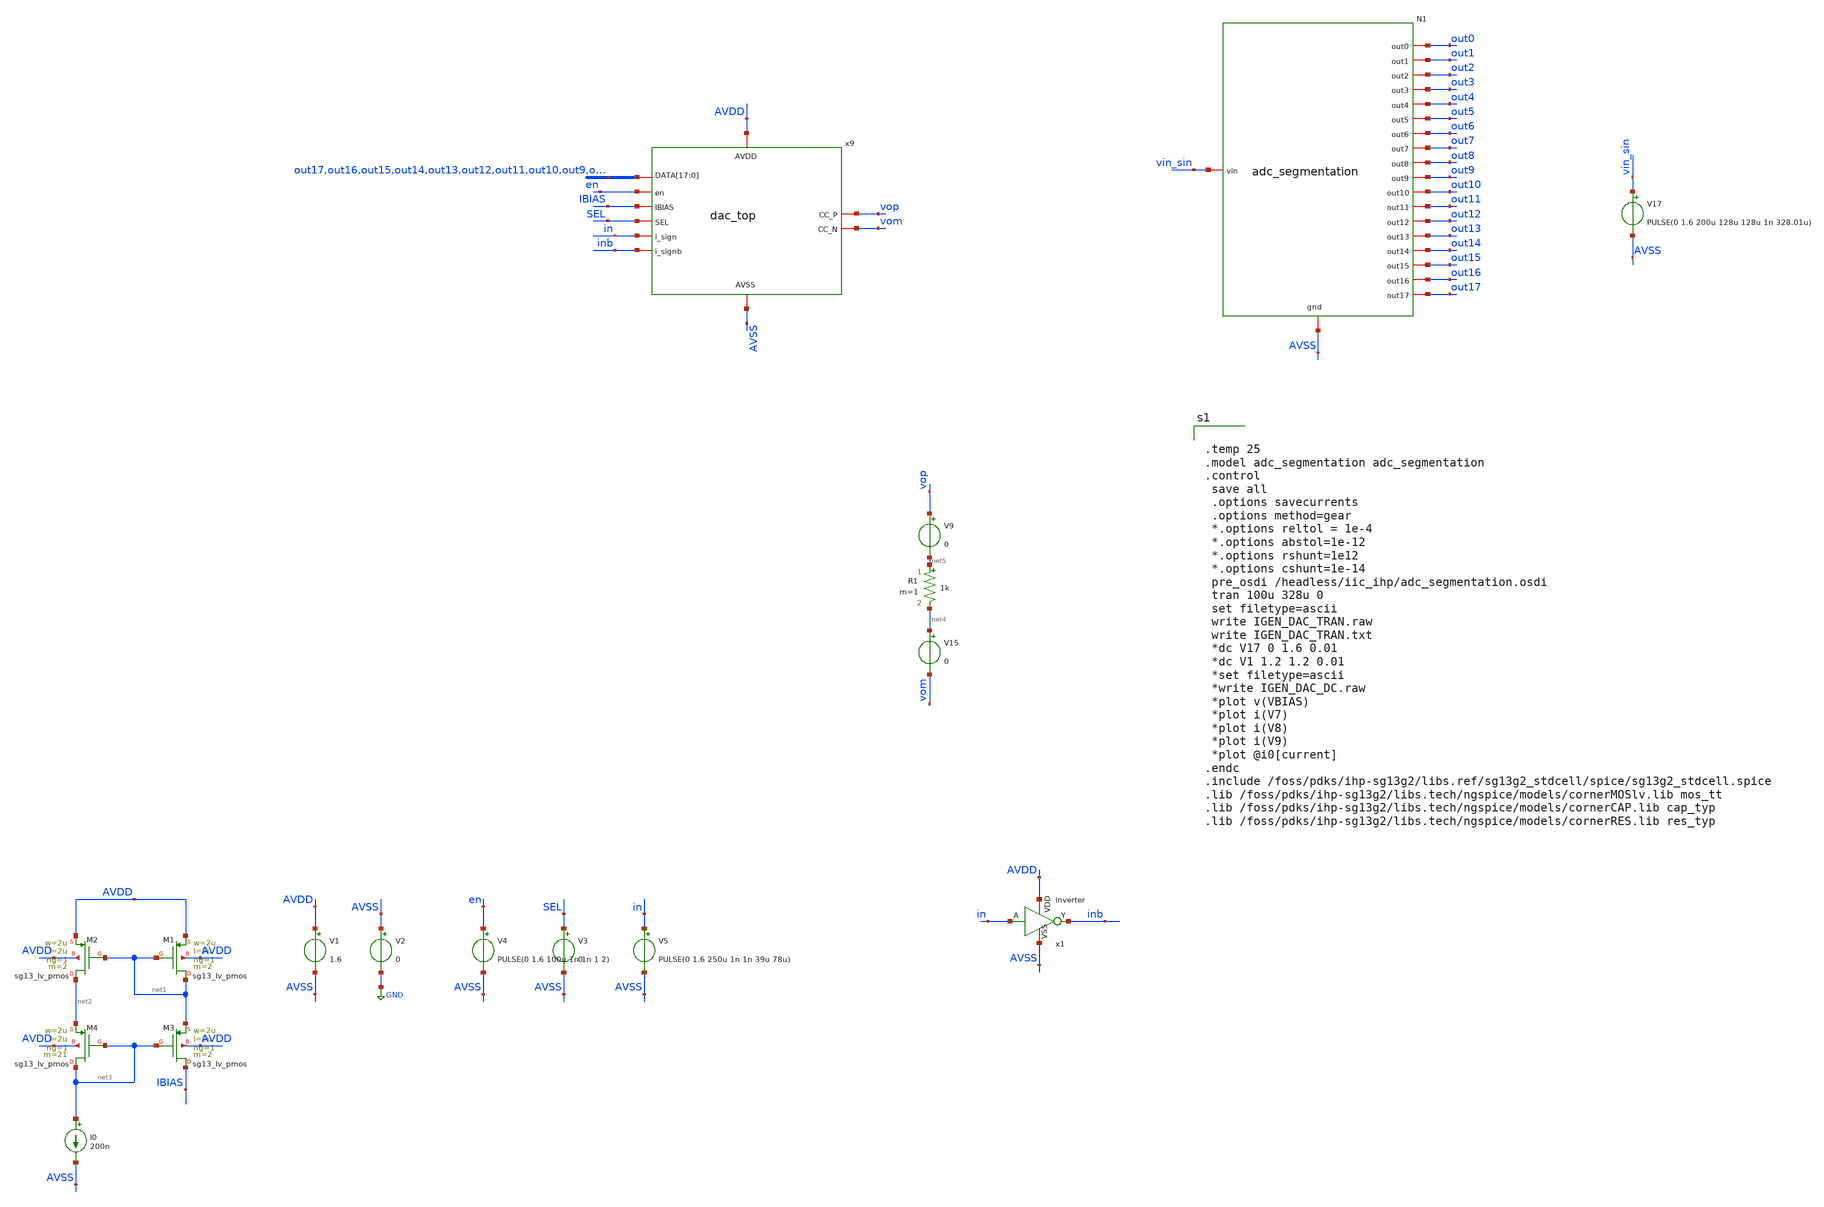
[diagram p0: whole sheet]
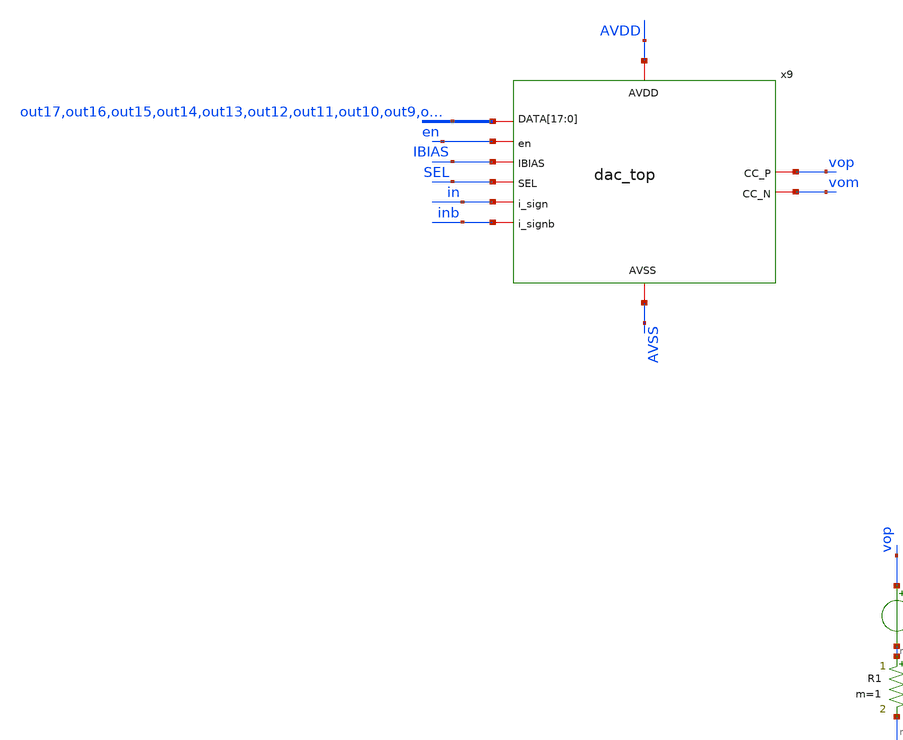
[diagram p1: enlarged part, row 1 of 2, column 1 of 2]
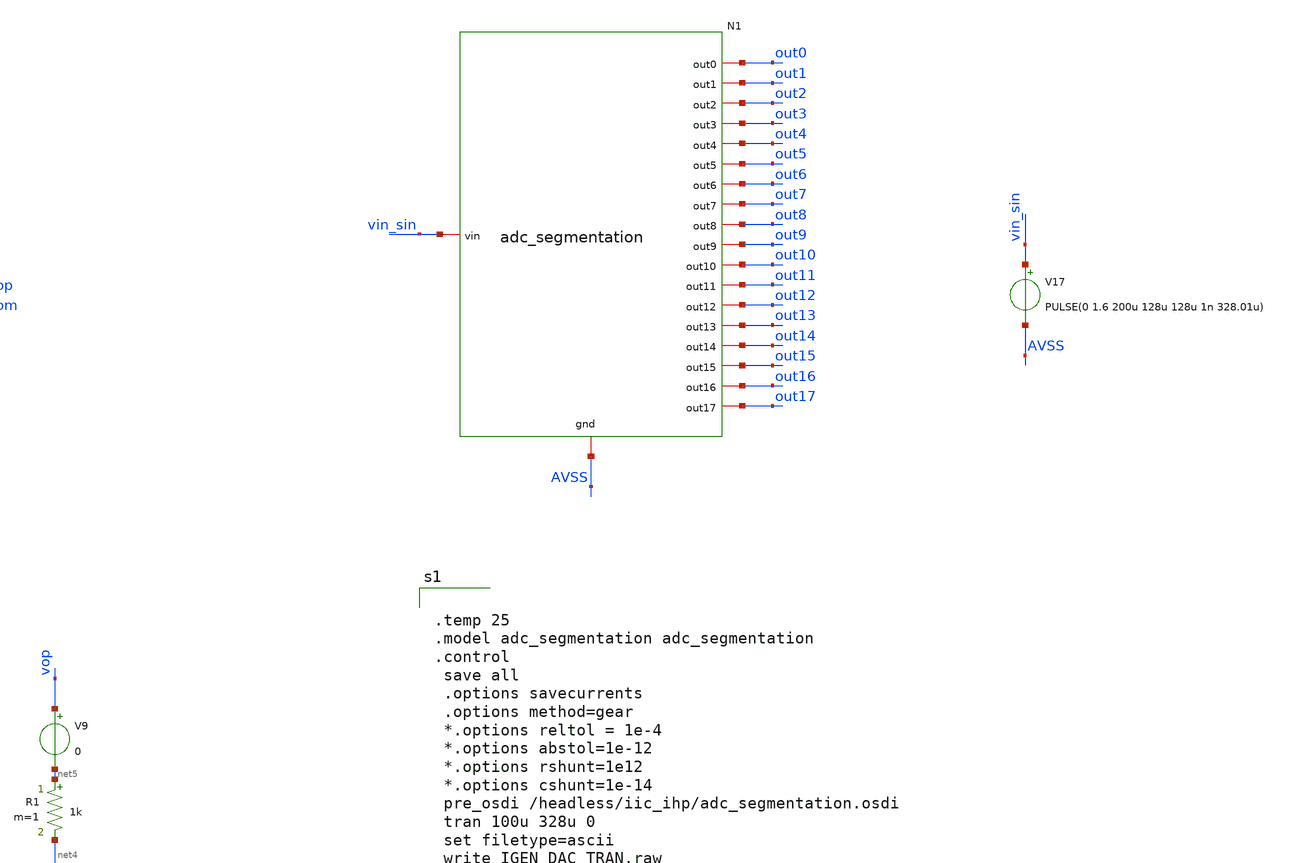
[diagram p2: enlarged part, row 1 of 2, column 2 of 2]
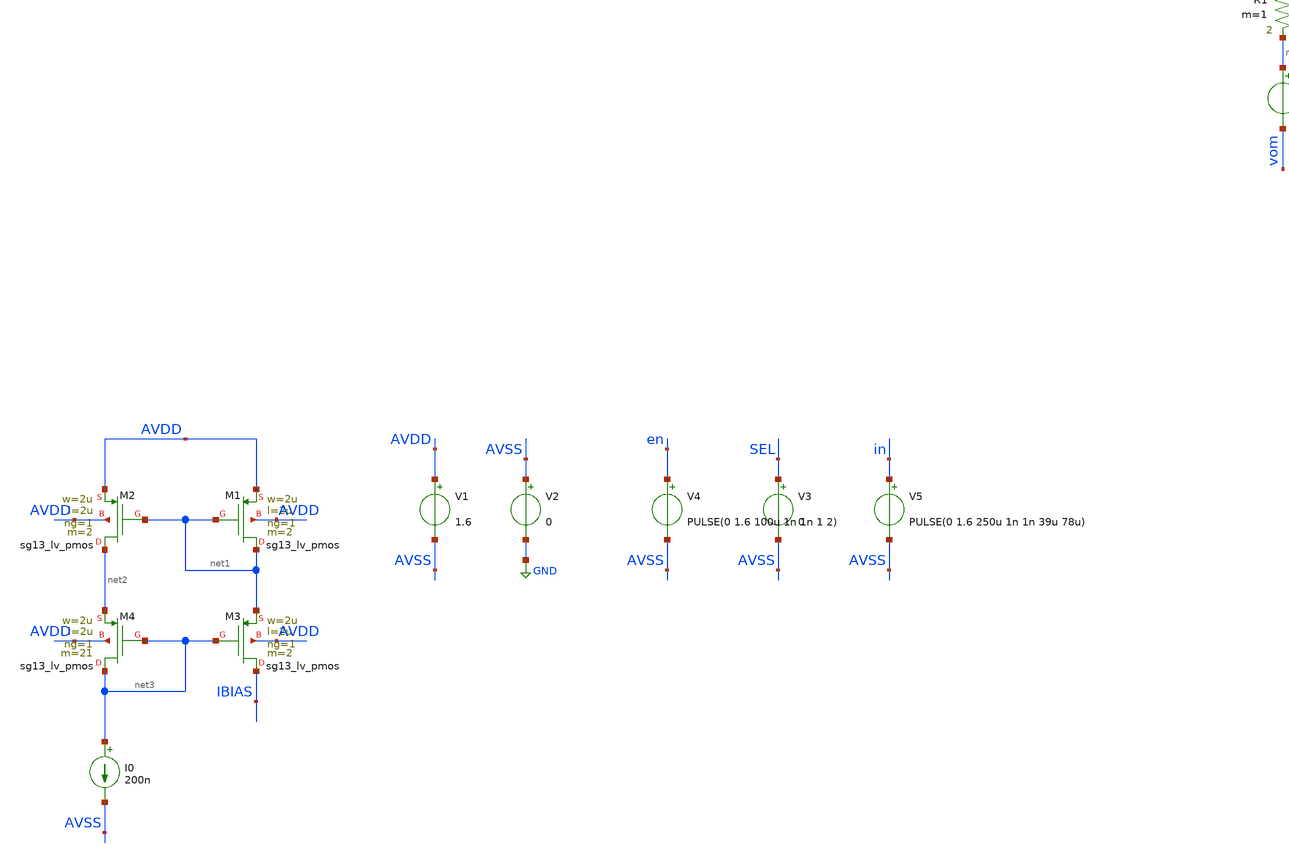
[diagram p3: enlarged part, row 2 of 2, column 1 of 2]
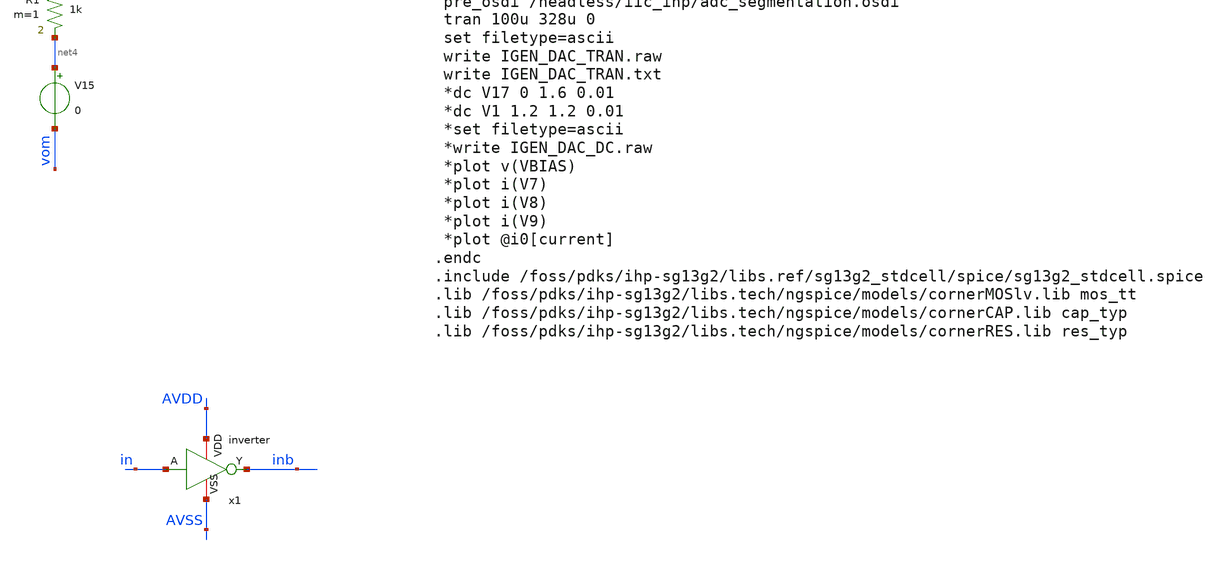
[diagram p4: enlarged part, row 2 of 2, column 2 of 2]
** sch_path: current_generator/analog/DAC/schematics/tb_dac_top.sch
**.subckt tb_dac_top
I0 net3 AVSS 200n
V1 AVDD AVSS 1.6
V2 AVSS GND 0
V3 SEL AVSS 0
XM1 net1 net1 AVDD AVDD sg13_lv_pmos w=2u l=2u ng=1 m=2 mm_ok=1
XM2 net2 net1 AVDD AVDD sg13_lv_pmos w=2u l=2u ng=1 m=2 mm_ok=1
XM3 IBIAS net3 net1 AVDD sg13_lv_pmos w=2u l=2u ng=1 m=2 mm_ok=1
XM4 net3 net3 net2 AVDD sg13_lv_pmos w=2u l=2u ng=1 m=21 mm_ok=1
N1 vin_sin AVSS out0 out10 out11 out1 out2 out12 out3 out13 out4 out14 out5 out15 out6 out16 out17
+ out7 out8 out9 adc_segmentation
V17 vin_sin AVSS PULSE(0 1.6 200u 128u 128u 1n 328.01u)
V4 en AVSS PULSE(0 1.6 100u 1n 1n 1 2)
V9 vop net5 0
V15 net4 vom 0
R1 net5 net4 1k m=1
x9 AVDD AVSS en out17 out16 out15 out14 out13 out12 out11 out10 out9 out8 out7 out6 out5 out4 out3
+ out2 out1 out0 IBIAS SEL in inb vop vom dac_top
x1 in inb AVDD AVSS inverter
V5 in AVSS PULSE(0 1.6 250u 1n 1n 39u 78u)
**** begin user architecture code


.temp 25
.model adc_segmentation adc_segmentation
.control
 save all
 .options savecurrents
 .options method=gear
 *.options reltol = 1e-4
 *.options abstol=1e-12
 *.options rshunt=1e12
 *.options cshunt=1e-14
 pre_osdi /headless/iic_ihp/adc_segmentation.osdi
 tran 100u 328u 0
 set filetype=ascii
 write IGEN_DAC_TRAN.raw
 write IGEN_DAC_TRAN.txt
 *dc V17 0 1.6 0.01
 *dc V1 1.2 1.2 0.01
 *set filetype=ascii
 *write IGEN_DAC_DC.raw
 *plot v(VBIAS)
 *plot i(V7)
 *plot i(V8)
 *plot i(V9)
 *plot @i0[current]
.endc
.include /foss/pdks/ihp-sg13g2/libs.ref/sg13g2_stdcell/spice/sg13g2_stdcell.spice
.lib /foss/pdks/ihp-sg13g2/libs.tech/ngspice/models/cornerMOSlv.lib mos_tt
.lib /foss/pdks/ihp-sg13g2/libs.tech/ngspice/models/cornerCAP.lib cap_typ
.lib /foss/pdks/ihp-sg13g2/libs.tech/ngspice/models/cornerRES.lib res_typ


**** end user architecture code
**.ends
.GLOBAL GND
.end
